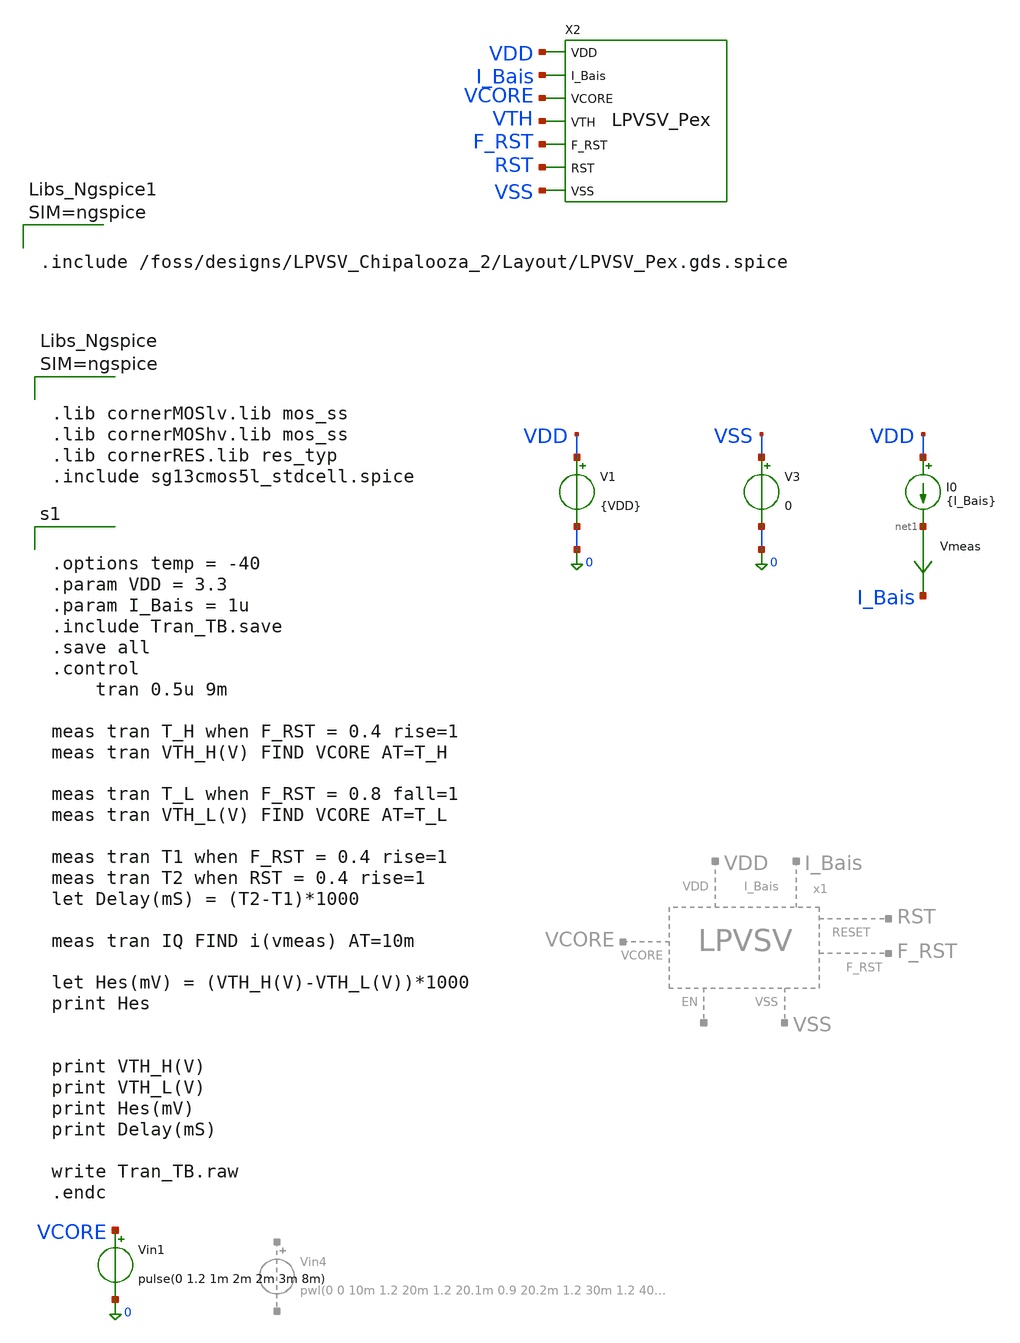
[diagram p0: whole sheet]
** sch_path: Simulation/Tran_TB.sch
**.subckt Tran_TB
I0 VDD net1 {I_Bais}
V1 VDD 0 {VDD}
V3 VSS 0 0
Vin1 VCORE 0 pulse(0 1.2 1m 2m 2m 3m 8m)
Vmeas net1 I_Bais 0
.save i(vmeas)
X2 F_RST VDD VCORE VSS I_Bais VTH RST LPVSV_Pex
**** begin user architecture code



.lib cornerMOSlv.lib mos_ss
.lib cornerMOShv.lib mos_ss
.lib cornerRES.lib res_typ
.include sg13cmos5l_stdcell.spice





.options temp = -40
.param VDD = 3.3
.param I_Bais = 1u
.include Tran_TB.save
.save all
.control
	tran 0.5u 9m

meas tran T_H when F_RST = 0.4 rise=1
meas tran VTH_H(V) FIND VCORE AT=T_H

meas tran T_L when F_RST = 0.8 fall=1
meas tran VTH_L(V) FIND VCORE AT=T_L

meas tran T1 when F_RST = 0.4 rise=1
meas tran T2 when RST = 0.4 rise=1
let Delay(mS) = (T2-T1)*1000

meas tran IQ FIND i(vmeas) AT=10m

let Hes(mV) = (VTH_H(V)-VTH_L(V))*1000
print Hes


print VTH_H(V)
print VTH_L(V)
print Hes(mV)
print Delay(mS)

write Tran_TB.raw
.endc





.include /foss/designs/LPVSV_Chipalooza_2/Layout/LPVSV_Pex.gds.spice



**** end user architecture code
**.ends
.end
